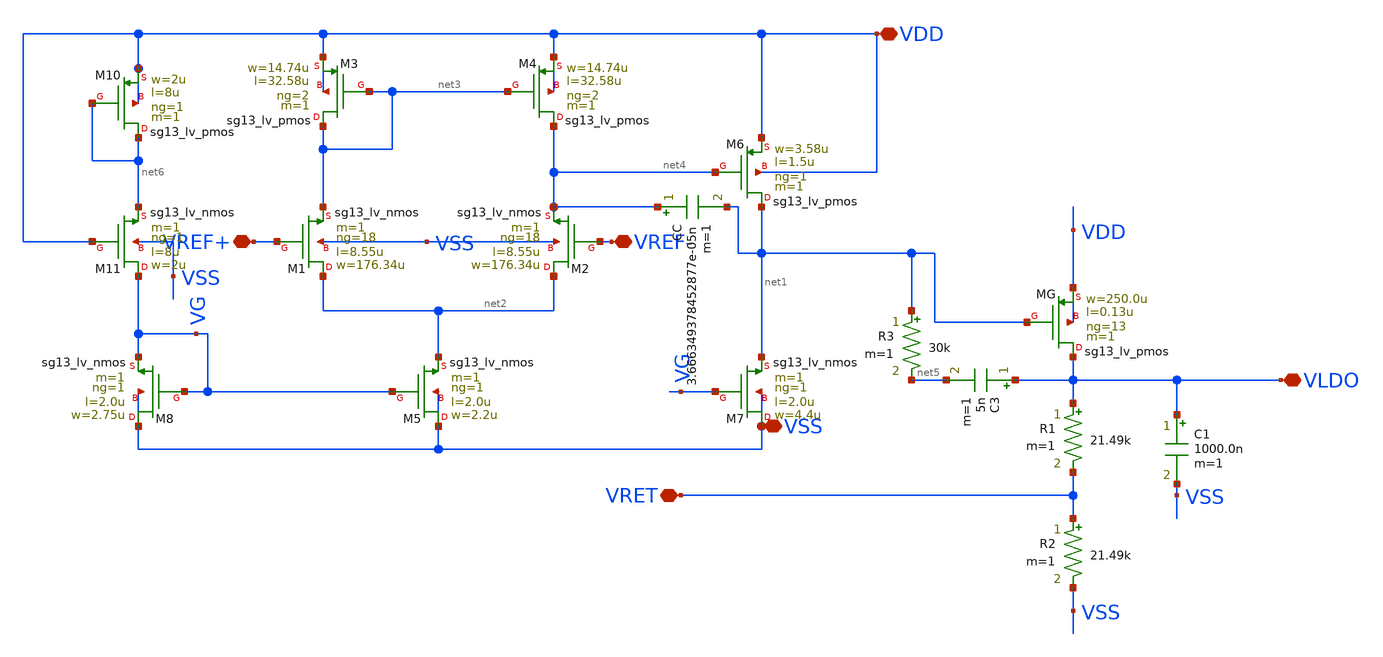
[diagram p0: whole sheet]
** sch_path: designs/1iee34/LDO1.sch
**.subckt LDO1 VREF+ VLDO VDD VREF- VSS VRET
*.iopin VREF+
*.iopin VLDO
*.iopin VDD
*.iopin VREF-
*.iopin VSS
*.iopin VRET
C1 VLDO VSS 1000.0n m=1
CC net4 net1 3.666349378452877e-05n m=1
R1 VLDO VRET 21.49k m=1
R2 VRET VSS 21.49k m=1
C3 VLDO net5 5n m=1
R3 net1 net5 30k m=1
XMG VLDO net1 VDD VDD sg13_lv_pmos w=250.0u l=0.13u ng=13 m=1 mm_ok=1
XM3 net3 net3 VDD VDD sg13_lv_pmos w=14.74u l=32.58u ng=2 m=1 mm_ok=1
XM4 net4 net3 VDD VDD sg13_lv_pmos w=14.74u l=32.58u ng=2 m=1 mm_ok=1
XM6 net1 net4 VDD VDD sg13_lv_pmos w=3.58u l=1.5u ng=1 m=1 mm_ok=1
XM1 net2 VREF+ net3 VSS sg13_lv_nmos w=176.34u l=8.55u ng=18 m=1 mm_ok=1
XM2 net2 VREF- net4 VSS sg13_lv_nmos w=176.34u l=8.55u ng=18 m=1 mm_ok=1
XM5 VSS VG net2 VSS sg13_lv_nmos w=2.2u l=2.0u ng=1 m=1 mm_ok=1
XM7 VSS VG net1 VSS sg13_lv_nmos w=4.4u l=2.0u ng=1 m=1 mm_ok=1
XM8 VSS VG VG VSS sg13_lv_nmos w=2.75u l=2.0u ng=1 m=1 mm_ok=1
XM10 net6 net6 VDD VDD sg13_lv_pmos w=2u l=8u ng=1 m=1 mm_ok=1
XM11 VG VDD net6 VSS sg13_lv_nmos w=2u l=8u ng=1 m=1 mm_ok=1
**.ends
.end
